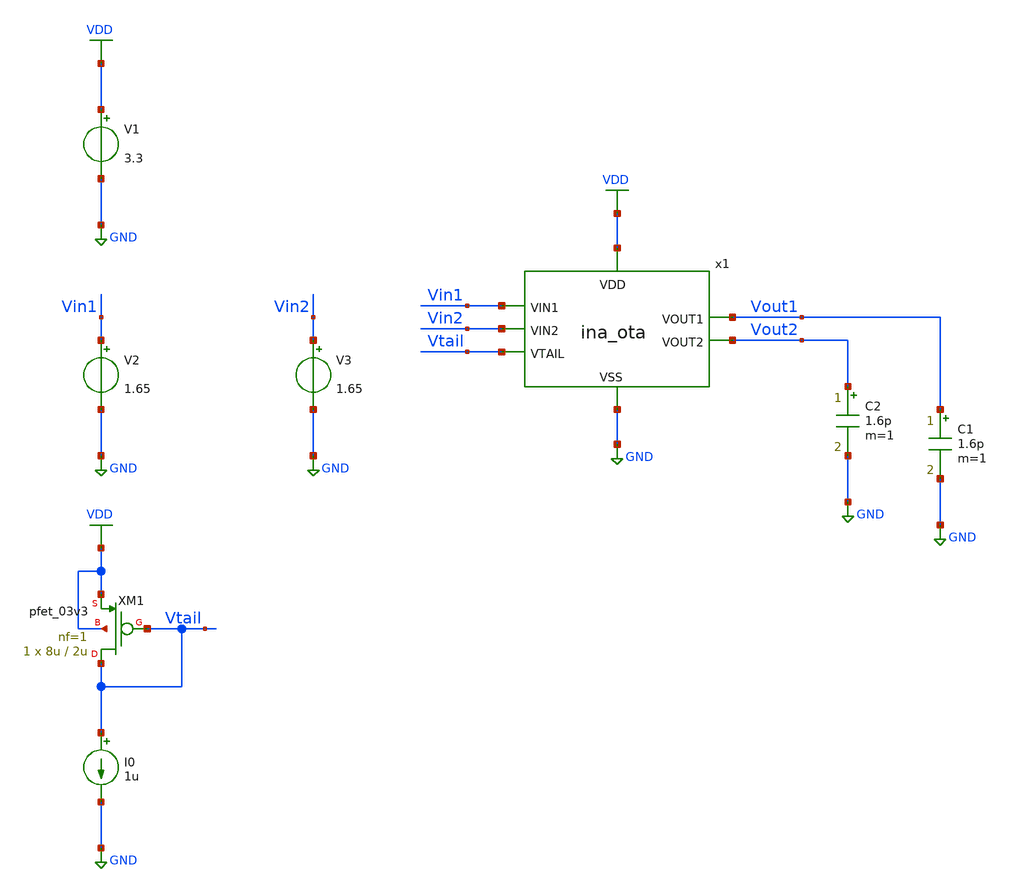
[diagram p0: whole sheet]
** sch_path: designs/libs/tb_ina/tb_ina_ota_stb/tb_ina_ota_stb.sch
**.subckt tb_ina_ota_stb
V1 VDD GND 3.3
V2 Vin1 GND 1.65
V3 Vin2 GND 1.65
C2 Vout2 GND 1.6p m=1
C1 Vout1 GND 1.6p m=1
XM1 Vtail Vtail VDD VDD pfet_03v3 L=2u W=8u nf=1 ad='int((nf+1)/2) * W/nf * 0.18u' as='int((nf+2)/2) * W/nf * 0.18u'
+ pd='2*int((nf+1)/2) * (W/nf + 0.18u)' ps='2*int((nf+2)/2) * (W/nf + 0.18u)' nrd='0.18u / W' nrs='0.18u / W'
+ sa=0 sb=0 sd=0 m=1
I0 Vtail GND 1u
x1 VDD Vtail Vin1 Vout2 Vout1 Vin2 GND ina_ota
**** begin user architecture code

.include $::180MCU_MODELS/design.ngspice
.lib $::180MCU_MODELS/sm141064.ngspice typical
.lib $::180MCU_MODELS/sm141064.ngspice cap_mim
.lib $::180MCU_MODELS/sm141064.ngspice moscap_typical
.lib $::180MCU_MODELS/sm141064.ngspice mimcap_typical
.lib $::180MCU_MODELS/sm141064.ngspice res_typical
* .lib $::180MCU_MODELS/sm141064.ngspice res_statistical
* ngspice commands




.control
save all

run
set color0 = white

*************************************
** PARAMETERS
*************************************

let Vdd  = 3.3
let Vcm  = 1.65
let Ibias = 2u

*************************************
** SOURCES
*************************************

alter @V1[DC] = $&Vdd
alter @V2[DC] = $&Vcm
alter @V3[DC] = $&Vcm
alter @V2[ACMAG] = 0.5
alter @V3[ACMAG] = -0.5
alter @I0[DC] = $&Ibias

*************************************
** AC SIMULATION
*************************************

ac dec 100 1 1G

*************************************
** MEASUREMENTS
*************************************

let vout_diff = v(Vout1)-v(Vout2)
let vin_diff  = v(Vin1)-v(Vin2)
let Av = vout_diff/vin_diff
let gain_db = db(Av)
let phase_deg = cph(-1*Av)*180/pi
meas ac UGF WHEN gain_db=0
meas ac phase_UGF FIND phase_deg WHEN gain_db=0
let PM = phase_UGF + 180
print PM

*************************************
** PLOTS
*************************************

setplot ac1
plot phase_deg

*************************************
** SAVE
*************************************

write tb_ina_ota_stb.raw

.endc
* ngspice commands



**** end user architecture code
**.ends

* expanding   symbol:  libs/core_ina/ina_ota/ina_ota.sym # of pins=7
** sym_path: designs/libs/core_ina/ina_ota/ina_ota.sym
** sch_path: designs/libs/core_ina/ina_ota/ina_ota.sch
.subckt ina_ota VDD VTAIL VIN1 VOUT2 VOUT1 VIN2 VSS
*.ipin Vin1
*.ipin Vin2
*.ipin Vtail
*.ipin VSS
*.opin Vout1
*.ipin VDD
*.opin Vout2
XM2 net4 net4 VDD VDD pfet_03v3 L=6u W=0.65u nf=1 ad='int((nf+1)/2) * W/nf * 0.18u' as='int((nf+2)/2) * W/nf * 0.18u'
+ pd='2*int((nf+1)/2) * (W/nf + 0.18u)' ps='2*int((nf+2)/2) * (W/nf + 0.18u)' nrd='0.18u / W' nrs='0.18u / W'
+ sa=0 sb=0 sd=0 m=1
XM1 net3 Vtail VDD VDD pfet_03v3 L=2u W=8u nf=1 ad='int((nf+1)/2) * W/nf * 0.18u' as='int((nf+2)/2) * W/nf * 0.18u'
+ pd='2*int((nf+1)/2) * (W/nf + 0.18u)' ps='2*int((nf+2)/2) * (W/nf + 0.18u)' nrd='0.18u / W' nrs='0.18u / W'
+ sa=0 sb=0 sd=0 m=1
XM3 net5 net5 VDD VDD pfet_03v3 L=6u W=0.65u nf=1 ad='int((nf+1)/2) * W/nf * 0.18u' as='int((nf+2)/2) * W/nf * 0.18u'
+ pd='2*int((nf+1)/2) * (W/nf + 0.18u)' ps='2*int((nf+2)/2) * (W/nf + 0.18u)' nrd='0.18u / W' nrs='0.18u / W'
+ sa=0 sb=0 sd=0 m=1
XM4 net1 Vin1 net3 VDD pfet_03v3 L=0.28u W=15u nf=1 ad='int((nf+1)/2) * W/nf * 0.18u' as='int((nf+2)/2) * W/nf * 0.18u'
+ pd='2*int((nf+1)/2) * (W/nf + 0.18u)' ps='2*int((nf+2)/2) * (W/nf + 0.18u)' nrd='0.18u / W' nrs='0.18u / W'
+ sa=0 sb=0 sd=0 m=10
XM5 net2 Vin2 net3 VDD pfet_03v3 L=0.28u W=15u nf=1 ad='int((nf+1)/2) * W/nf * 0.18u' as='int((nf+2)/2) * W/nf * 0.18u'
+ pd='2*int((nf+1)/2) * (W/nf + 0.18u)' ps='2*int((nf+2)/2) * (W/nf + 0.18u)' nrd='0.18u / W' nrs='0.18u / W'
+ sa=0 sb=0 sd=0 m=10
XM6 net4 net1 VSS VSS nfet_03v3 L=6u W=1.8u nf=1 ad='int((nf+1)/2) * W/nf * 0.18u' as='int((nf+2)/2) * W/nf * 0.18u'
+ pd='2*int((nf+1)/2) * (W/nf + 0.18u)' ps='2*int((nf+2)/2) * (W/nf + 0.18u)' nrd='0.18u / W' nrs='0.18u / W'
+ sa=0 sb=0 sd=0 m=1
XM7 net5 net2 VSS VSS nfet_03v3 L=6u W=1.8u nf=1 ad='int((nf+1)/2) * W/nf * 0.18u' as='int((nf+2)/2) * W/nf * 0.18u'
+ pd='2*int((nf+1)/2) * (W/nf + 0.18u)' ps='2*int((nf+2)/2) * (W/nf + 0.18u)' nrd='0.18u / W' nrs='0.18u / W'
+ sa=0 sb=0 sd=0 m=1
XM8 net1 net1 VSS VSS nfet_03v3 L=6u W=1.8u nf=1 ad='int((nf+1)/2) * W/nf * 0.18u' as='int((nf+2)/2) * W/nf * 0.18u'
+ pd='2*int((nf+1)/2) * (W/nf + 0.18u)' ps='2*int((nf+2)/2) * (W/nf + 0.18u)' nrd='0.18u / W' nrs='0.18u / W'
+ sa=0 sb=0 sd=0 m=1
XM9 net2 net2 VSS VSS nfet_03v3 L=6u W=1.8u nf=1 ad='int((nf+1)/2) * W/nf * 0.18u' as='int((nf+2)/2) * W/nf * 0.18u'
+ pd='2*int((nf+1)/2) * (W/nf + 0.18u)' ps='2*int((nf+2)/2) * (W/nf + 0.18u)' nrd='0.18u / W' nrs='0.18u / W'
+ sa=0 sb=0 sd=0 m=1
XM10 Vout1 net4 VDD VDD pfet_03v3 L=6u W=0.65u nf=1 ad='int((nf+1)/2) * W/nf * 0.18u' as='int((nf+2)/2) * W/nf * 0.18u'
+ pd='2*int((nf+1)/2) * (W/nf + 0.18u)' ps='2*int((nf+2)/2) * (W/nf + 0.18u)' nrd='0.18u / W' nrs='0.18u / W'
+ sa=0 sb=0 sd=0 m=1
XM11 Vout1 net2 VSS VSS nfet_03v3 L=6u W=1.8u nf=1 ad='int((nf+1)/2) * W/nf * 0.18u' as='int((nf+2)/2) * W/nf * 0.18u'
+ pd='2*int((nf+1)/2) * (W/nf + 0.18u)' ps='2*int((nf+2)/2) * (W/nf + 0.18u)' nrd='0.18u / W' nrs='0.18u / W'
+ sa=0 sb=0 sd=0 m=1
XM12 Vout2 net1 VSS VSS nfet_03v3 L=6u W=1.8u nf=1 ad='int((nf+1)/2) * W/nf * 0.18u' as='int((nf+2)/2) * W/nf * 0.18u'
+ pd='2*int((nf+1)/2) * (W/nf + 0.18u)' ps='2*int((nf+2)/2) * (W/nf + 0.18u)' nrd='0.18u / W' nrs='0.18u / W'
+ sa=0 sb=0 sd=0 m=1
XM13 Vout2 net5 VDD VDD pfet_03v3 L=6u W=0.65u nf=1 ad='int((nf+1)/2) * W/nf * 0.18u' as='int((nf+2)/2) * W/nf * 0.18u'
+ pd='2*int((nf+1)/2) * (W/nf + 0.18u)' ps='2*int((nf+2)/2) * (W/nf + 0.18u)' nrd='0.18u / W' nrs='0.18u / W'
+ sa=0 sb=0 sd=0 m=1
.ends

.GLOBAL GND
.GLOBAL VDD
.end
